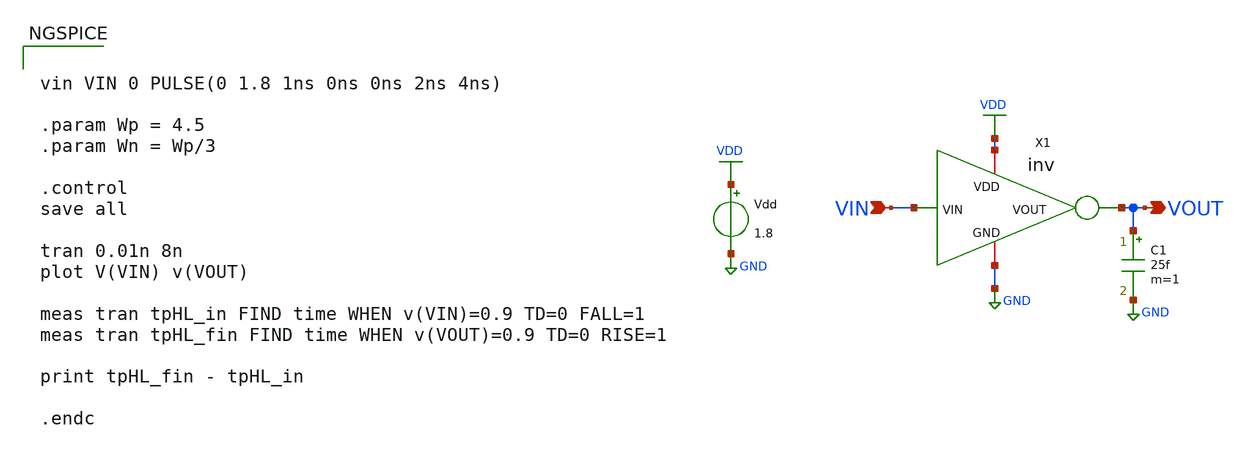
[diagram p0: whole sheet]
** sch_path: resuelto/schematic/inv_tb.sch
**.subckt inv_tb VIN VOUT
*.ipin VIN
*.opin VOUT
Vdd VDD GND 1.8
C1 VOUT GND 25f m=1
X1 VDD VIN VOUT GND inv
**** begin user architecture code

vin VIN 0 PULSE(0 1.8 1ns 0ns 0ns 2ns 4ns)

.param Wp = 4.5
.param Wn = Wp/3

.control
save all

tran 0.01n 8n
plot V(VIN) v(VOUT)

meas tran tpHL_in FIND time WHEN v(VIN)=0.9 TD=0 FALL=1
meas tran tpHL_fin FIND time WHEN v(VOUT)=0.9 TD=0 RISE=1

print tpHL_fin - tpHL_in

.endc


.lib $env(PDK_ROOT)/$env(PDK)/libs.tech/ngspice/sky130.lib.spice tt

**** end user architecture code
**.ends

* expanding   symbol:  inv.sym # of pins=4
** sym_path: resuelto/schematic/inv.sym
** sch_path: resuelto/schematic/inv.sch
.subckt inv VDD VIN VOUT GND
*.iopin VDD
*.iopin GND
*.ipin VIN
*.opin VOUT
XM1 VOUT VIN GND GND sky130_fd_pr__nfet_01v8 L=0.3 W={Wn} nf=1 ad='int((nf+1)/2) * W/nf * 0.29' as='int((nf+2)/2) * W/nf * 0.29'
+ pd='2*int((nf+1)/2) * (W/nf + 0.29)' ps='2*int((nf+2)/2) * (W/nf + 0.29)' nrd='0.29 / W' nrs='0.29 / W'
+ sa=0 sb=0 sd=0 mult=1 m=1
XM2 VOUT VIN VDD VDD sky130_fd_pr__pfet_01v8 L=0.3 W={Wp} nf=1 ad='int((nf+1)/2) * W/nf * 0.29' as='int((nf+2)/2) * W/nf * 0.29'
+ pd='2*int((nf+1)/2) * (W/nf + 0.29)' ps='2*int((nf+2)/2) * (W/nf + 0.29)' nrd='0.29 / W' nrs='0.29 / W'
+ sa=0 sb=0 sd=0 mult=1 m=1
.ends

.GLOBAL VDD
.GLOBAL GND
.end
